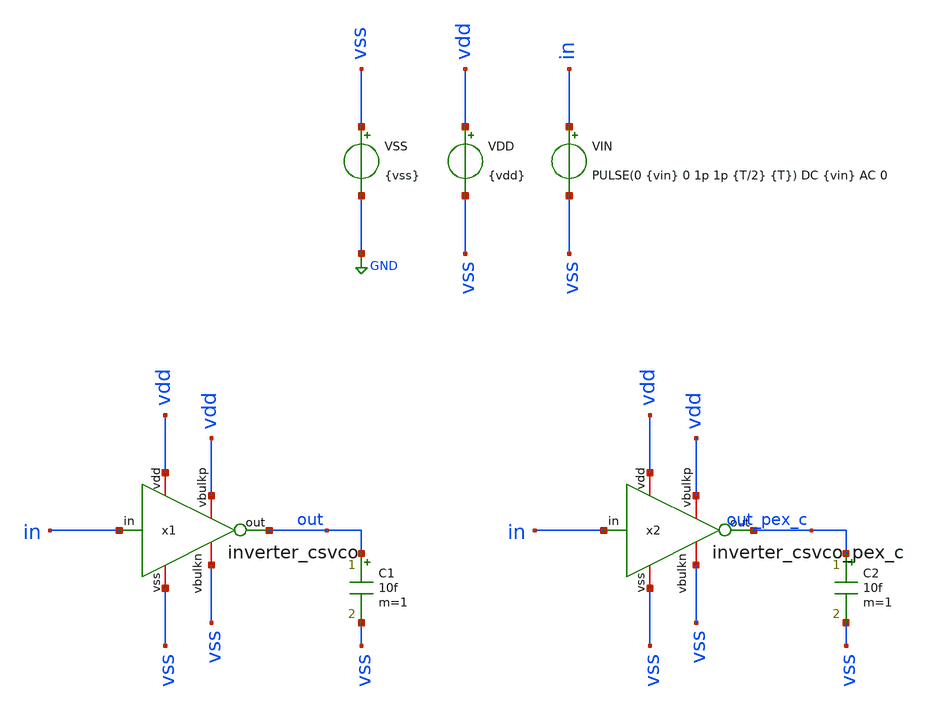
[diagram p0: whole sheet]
** sch_path: xschem/tb_inverter_csvco.sch
**.subckt tb_inverter_csvco
VSS vss GND {vss}
VDD vdd vss {vdd}
VIN in vss PULSE(0 {vin} 0 1p 1p {T/2} {T}) DC {vin} AC 0
C1 out vss 10f m=1
x1 vdd out in vss vdd vss inverter_csvco
x2 vdd out_pex_c in vss vdd vss inverter_csvco_pex_c
C2 out_pex_c vss 10f m=1
**** begin user architecture code



* Parameters
.param kp = 1.0
.param vdd = kp*1.8
.param vss = 0
.param vin = vdd
.param T   = 100n

.options TEMP = 50.0

* Models
.lib ~/skywater/skywater-pdk/libraries/sky130_fd_pr_ngspice/latest/models/corners/sky130.lib TT
.include ~/sky130-mpw2-fulgor/inverter_csvco/sch/simulations/inverter_csvco_pex_c.spice

* Initial Conditions
.ic v(out) = 0.0
.ic v(out_wp) = 0.0
.ic v(out_wp_rc) = 0.0
.ic v(out_pex_c) = 0.0

* Data to save
.save all  @M.X1.XM1.msky130_fd_pr__nfet_01v8[id]  @M.X1.XM2.msky130_fd_pr__pfet_01v8[id]  @M.X1.XM1.msky130_fd_pr__nfet_01v8[vds]  @M.X1.XM2.msky130_fd_pr__pfet_01v8[vds]  @M.X1.XM1.msky130_fd_pr__nfet_01v8[vdsat]  @M.X1.XM2.msky130_fd_pr__pfet_01v8[vdsat]  @M.X1.XM1.msky130_fd_pr__nfet_01v8[cgs]  @M.X1.XM2.msky130_fd_pr__pfet_01v8[cgs]  @M.X1.XM1.msky130_fd_pr__nfet_01v8[cgd]  @M.X1.XM2.msky130_fd_pr__pfet_01v8[cgd]  @M.X1.XM1.msky130_fd_pr__nfet_01v8[csb]  @M.X1.XM2.msky130_fd_pr__pfet_01v8[csb]  @M.X1.XM1.msky130_fd_pr__nfet_01v8[cdb]  @M.X1.XM2.msky130_fd_pr__pfet_01v8[cdb]  @M.X1.XM1.msky130_fd_pr__nfet_01v8[cgg]  @M.X1.XM2.msky130_fd_pr__pfet_01v8[cgg]  @M.X1.XM1.msky130_fd_pr__nfet_01v8[cgb]  @M.X1.XM2.msky130_fd_pr__pfet_01v8[cgb]

* Simulation
.control
	set filetype = ascii
	op
	write tb_inverter_min.raw
	echo .
	echo ------ OP Results -----
	print all

	reset

	dc vin 0 1.8 0.01
	setplot dc1
	plot v(in) v(out) v(out_pex_c)
	write tb_inverter_min_dc.raw

	reset

	tran 1ns 1us
	meas tran tpLH trig v(in) val=0.9 fall=5 targ v(out) val=0.9 rise=5
	meas tran tpHL trig v(in) val=0.9 rise=5 targ v(out) val=0.9 fall=4
	meas tran tpLHc trig v(in) val=0.9 fall=5 targ v(out_pex_c) val=0.9 rise=5
	meas tran tpHLc trig v(in) val=0.9 rise=5 targ v(out_pex_c) val=0.9 fall=4
	let tp = (0.5*(tpLH + tpHL))
	let tp_c = (0.5*(tpLHc + tpHLc))
	echo .
	echo ---- tp Ideal ----
	print tpLH tpHL tp
	echo .
	echo ---- tp PEX C ----
	print tpLHc tpHLc tp_c
	write tb_inverter_tran.raw
	plot v(in) v(out) v(out_pex_c)+2

.endc

.end


**** end user architecture code
**.ends

* expanding   symbol:  inverter_csvco.sym # of pins=6
** sym_path: xschem/inverter_csvco.sym
** sch_path: xschem/inverter_csvco.sch
.subckt inverter_csvco vdd out in vss vbulkp vbulkn
*.iopin vss
*.ipin in
*.opin out
*.iopin vdd
*.iopin vbulkn
*.iopin vbulkp
XM1 out in vss vbulkn sky130_fd_pr__nfet_01v8 L=0.2 W=0.75 nf=1 ad='int((nf+1)/2) * W/nf * 0.29' as='int((nf+2)/2) * W/nf * 0.29'
+ pd='2*int((nf+1)/2) * (W/nf + 0.29)' ps='2*int((nf+2)/2) * (W/nf + 0.29)' nrd='0.29 / W' nrs='0.29 / W'
+ sa=0 sb=0 sd=0 mult=1 m=1
XM2 out in vdd vbulkp sky130_fd_pr__pfet_01v8 L=0.2 W=1.5 nf=1 ad='int((nf+1)/2) * W/nf * 0.29' as='int((nf+2)/2) * W/nf * 0.29'
+ pd='2*int((nf+1)/2) * (W/nf + 0.29)' ps='2*int((nf+2)/2) * (W/nf + 0.29)' nrd='0.29 / W' nrs='0.29 / W'
+ sa=0 sb=0 sd=0 mult=1 m=1
.ends

.GLOBAL GND
.end
